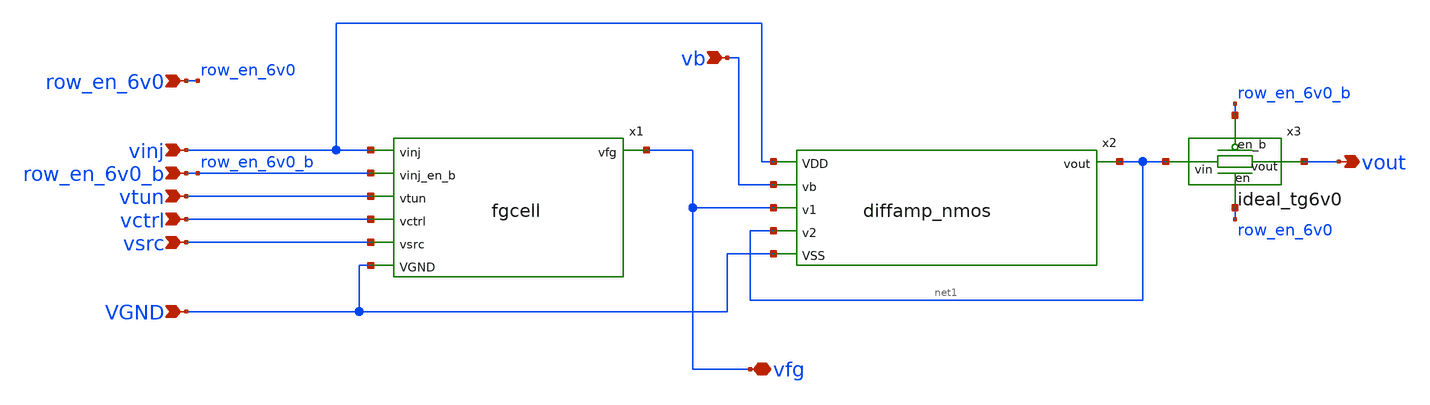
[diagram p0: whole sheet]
** sch_path: xschem/fgcell_amp.sch
**.subckt fgcell_amp vinj row_en_6v0_b vtun vctrl vsrc vb VGND vout vfg row_en_6v0
*.ipin vinj
*.ipin row_en_6v0_b
*.ipin vtun
*.ipin vctrl
*.ipin vsrc
*.ipin vb
*.ipin VGND
*.opin vout
*.iopin vfg
*.ipin row_en_6v0
x3 net1 vout row_en_6v0 row_en_6v0_b ideal_tg6v0
x1 vctrl vtun vinj row_en_6v0_b vsrc vfg VGND fgcell
x2 vinj vb net1 vfg net1 VGND diffamp_nmos
**.ends

* expanding   symbol:  ideal_tg6v0.sym # of pins=4
** sym_path: xschem/ideal_tg6v0.sym
** sch_path: xschem/ideal_tg6v0.sch
.subckt ideal_tg6v0 vin vout en en_b
*.ipin vin
*.ipin en_b
*.opin vout
*.ipin en
**** begin user architecture code


.model sw_vinj SW vt=3 vh=0.1 ron=14k roff=10gig
.model sw_1v8 SW vt={1.8/2}  vh=0.1 ron=10k roff=10gig


**** end user architecture code
S1 vin vout en en_b sw_vinj
.ends

.end
